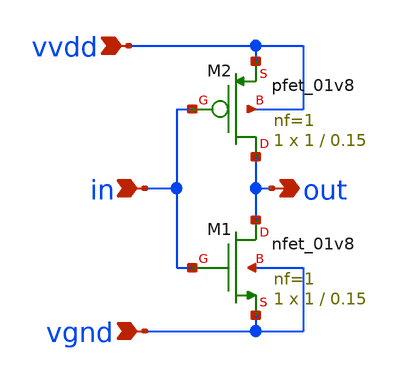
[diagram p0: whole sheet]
** sch_path: ring_oscillator/inverter.sch
**.subckt inverter vvdd in vgnd out
*.ipin vvdd
*.ipin in
*.ipin vgnd
*.opin out
XM1 out in vgnd vgnd sky130_fd_pr__nfet_01v8 L=0.15 W=1 nf=1 ad='int((nf+1)/2) * W/nf * 0.29' as='int((nf+2)/2) * W/nf * 0.29'
+ pd='2*int((nf+1)/2) * (W/nf + 0.29)' ps='2*int((nf+2)/2) * (W/nf + 0.29)' nrd='0.29 / W' nrs='0.29 / W'
+ sa=0 sb=0 sd=0 mult=1 m=1
XM2 out in vvdd vvdd sky130_fd_pr__pfet_01v8 L=0.15 W=1 nf=1 ad='int((nf+1)/2) * W/nf * 0.29' as='int((nf+2)/2) * W/nf * 0.29'
+ pd='2*int((nf+1)/2) * (W/nf + 0.29)' ps='2*int((nf+2)/2) * (W/nf + 0.29)' nrd='0.29 / W' nrs='0.29 / W'
+ sa=0 sb=0 sd=0 mult=1 m=1
**.ends
.end
